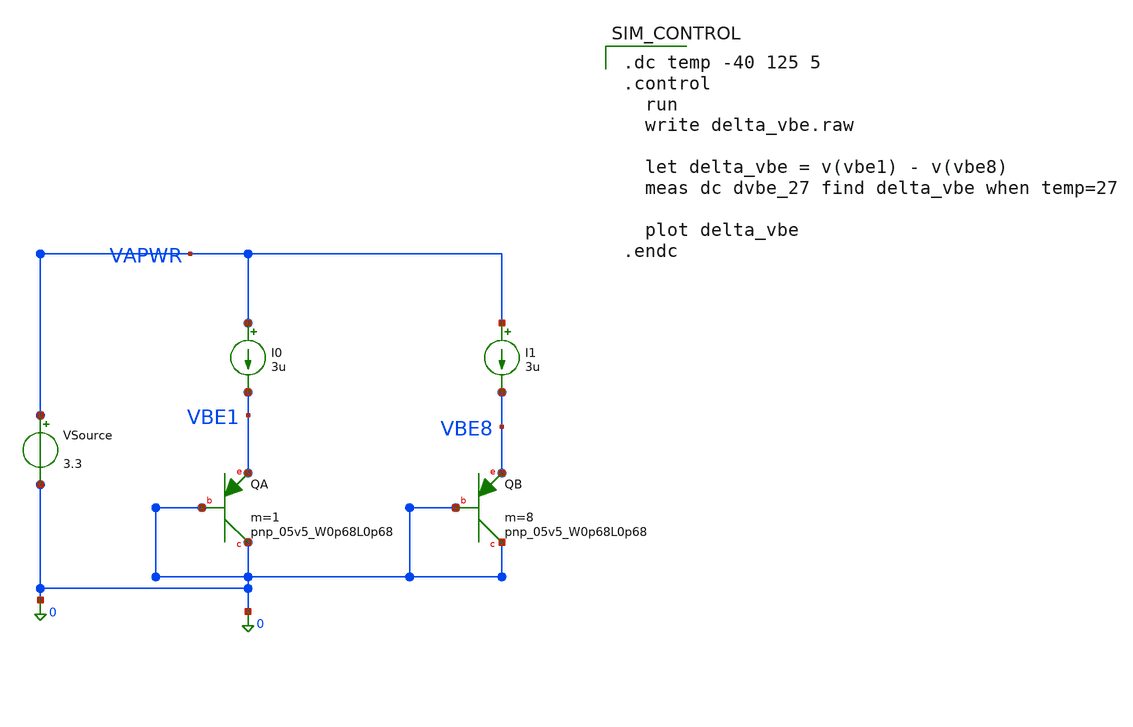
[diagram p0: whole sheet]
** sch_path: designs/bgr_ldo/sim/delta_vbe.sch
**.subckt delta_vbe
XQA 0 0 VBE1 sky130_fd_pr__pnp_05v5_W0p68L0p68 m=1
VSource VAPWR 0 3.3
I0 VAPWR VBE1 3u
XQB 0 0 VBE8 sky130_fd_pr__pnp_05v5_W0p68L0p68 m=8
I1 VAPWR VBE8 3u
**** begin user architecture code

.dc temp -40 125 5
.control
  run
  write delta_vbe.raw

  let delta_vbe = v(vbe1) - v(vbe8)
  meas dc dvbe_27 find delta_vbe when temp=27

  plot delta_vbe
.endc


** opencircuitdesign pdks install
.lib $::SKYWATER_MODELS/sky130.lib.spice tt

**** end user architecture code
**.ends
.end
